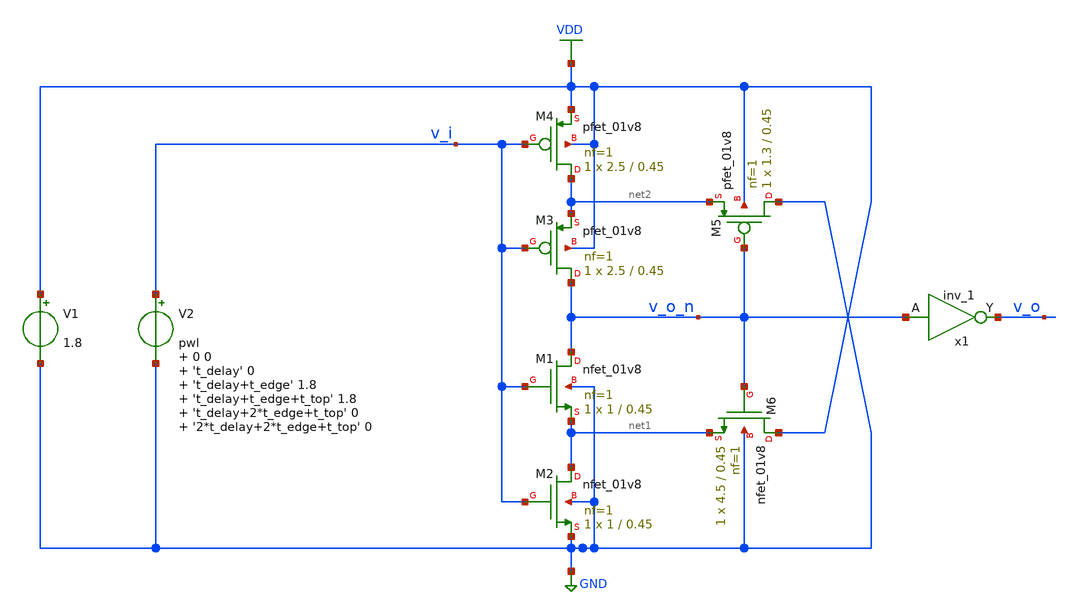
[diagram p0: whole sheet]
** sch_path: ngspice-meas-table-single.sch
.lib $::SKYWATER_MODELS/sky130.lib.spice tt
.include $::SKYWATER_STDCELLS/sky130_fd_sc_hd.spice
**.subckt ngspice-meas-table-single
V1 VDD GND 1.8
V2 v_i GND pwl 0 0 't_delay' 0 't_delay+t_edge' 1.8 't_delay+t_edge+t_top' 1.8 't_delay+2*t_edge+t_top'
+ 0 '2*t_delay+2*t_edge+t_top' 0
x1 v_o_n GND GND VDD VDD v_o sky130_fd_sc_hd__inv_1
XM4 net2 v_i VDD VDD sky130_fd_pr__pfet_01v8 L=0.45 W=2.5 nf=1 ad='int((nf+1)/2) * W/nf * 0.29' as='int((nf+2)/2) * W/nf * 0.29'
+ pd='2*int((nf+1)/2) * (W/nf + 0.29)' ps='2*int((nf+2)/2) * (W/nf + 0.29)' nrd='0.29 / W' nrs='0.29 / W'
+ sa=0 sb=0 sd=0 mult=1 m=1
XM5 GND v_o_n net2 VDD sky130_fd_pr__pfet_01v8 L=0.45 W=1.3 nf=1 ad='int((nf+1)/2) * W/nf * 0.29' as='int((nf+2)/2) * W/nf * 0.29'
+ pd='2*int((nf+1)/2) * (W/nf + 0.29)' ps='2*int((nf+2)/2) * (W/nf + 0.29)' nrd='0.29 / W' nrs='0.29 / W'
+ sa=0 sb=0 sd=0 mult=1 m=1
XM6 VDD v_o_n net1 GND sky130_fd_pr__nfet_01v8 L=0.45 W=4.5 nf=1 ad='int((nf+1)/2) * W/nf * 0.29' as='int((nf+2)/2) * W/nf * 0.29'
+ pd='2*int((nf+1)/2) * (W/nf + 0.29)' ps='2*int((nf+2)/2) * (W/nf + 0.29)' nrd='0.29 / W' nrs='0.29 / W'
+ sa=0 sb=0 sd=0 mult=1 m=1
XM1 v_o_n v_i net1 GND sky130_fd_pr__nfet_01v8 L=0.45 W=1 nf=1 ad='int((nf+1)/2) * W/nf * 0.29' as='int((nf+2)/2) * W/nf * 0.29'
+ pd='2*int((nf+1)/2) * (W/nf + 0.29)' ps='2*int((nf+2)/2) * (W/nf + 0.29)' nrd='0.29 / W' nrs='0.29 / W'
+ sa=0 sb=0 sd=0 mult=1 m=1
XM2 net1 v_i GND GND sky130_fd_pr__nfet_01v8 L=0.45 W=1 nf=1 ad='int((nf+1)/2) * W/nf * 0.29' as='int((nf+2)/2) * W/nf * 0.29'
+ pd='2*int((nf+1)/2) * (W/nf + 0.29)' ps='2*int((nf+2)/2) * (W/nf + 0.29)' nrd='0.29 / W' nrs='0.29 / W'
+ sa=0 sb=0 sd=0 mult=1 m=1
XM3 v_o_n v_i net2 VDD sky130_fd_pr__pfet_01v8 L=0.45 W=2.5 nf=1 ad='int((nf+1)/2) * W/nf * 0.29' as='int((nf+2)/2) * W/nf * 0.29'
+ pd='2*int((nf+1)/2) * (W/nf + 0.29)' ps='2*int((nf+2)/2) * (W/nf + 0.29)' nrd='0.29 / W' nrs='0.29 / W'
+ sa=0 sb=0 sd=0 mult=1 m=1
**** begin user architecture code


.param t_delay=1n
.param t_edge=10p
.param t_top=1n
.control
	save all

	setplot new
	set myplot=$curplot
	let t_pd_l2h=vector(1)
	let t_pd_h2l=vector(1)

	tran 0.1p 3n

	MEAS TRAN t_pd_L2H TRIG V(v_i) VAL=0.9 RISE=1 TARG V(v_o) VAL=0.9 RISE=1
	MEAS TRAN t_pd_H2L TRIG V(v_i) VAL=0.9 FALL=1 TARG V(v_o) VAL=0.9 FALL=1

	let {$myplot}.t_pd_l2h[0]=t_pd_l2h
	let {$myplot}.t_pd_h2l[0]=t_pd_h2l

	write ngspice-meas-table-single.raw

	setplot $myplot
	settype time t_pd_l2h
	settype time t_pd_h2l
	write ngspice-meas-table-single-meas.raw
.endc


**** end user architecture code
**.ends
.GLOBAL GND
.GLOBAL VDD
.end
